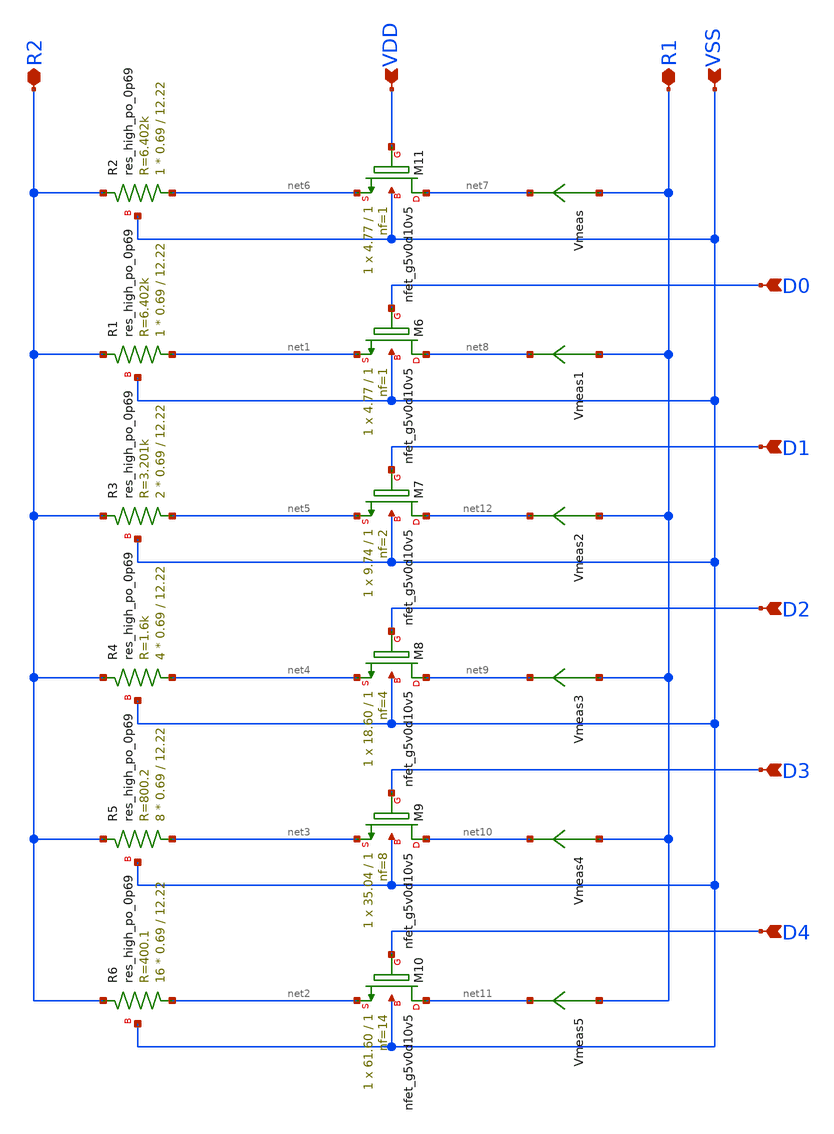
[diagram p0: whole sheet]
** sch_path: xschem/RB_array_20.sch
**.subckt RB_array_20 VSS R2 D0 D1 D2 D3 D4 R1 VDD
*.ipin VSS
*.iopin R2
*.ipin D0
*.ipin D1
*.ipin D2
*.ipin D3
*.ipin D4
*.iopin R1
*.ipin VDD
XR2 net6 R2 VSS sky130_fd_pr__res_high_po_0p69 L=12.22 mult=1 m=1
XR1 net1 R2 VSS sky130_fd_pr__res_high_po_0p69 L=12.22 mult=1 m=1
XR3 net5 R2 VSS sky130_fd_pr__res_high_po_0p69 L=12.22 mult=2 m=2
XR4 net4 R2 VSS sky130_fd_pr__res_high_po_0p69 L=12.22 mult=4 m=4
XR5 net3 R2 VSS sky130_fd_pr__res_high_po_0p69 L=12.22 mult=8 m=8
XR6 net2 R2 VSS sky130_fd_pr__res_high_po_0p69 L=12.22 mult=16 m=16
XM6 net8 D0 net1 VSS sky130_fd_pr__nfet_g5v0d10v5 L=1 W=4.77 nf=1 ad='int((nf+1)/2) * W/nf * 0.29' as='int((nf+2)/2) * W/nf * 0.29'
+ pd='2*int((nf+1)/2) * (W/nf + 0.29)' ps='2*int((nf+2)/2) * (W/nf + 0.29)' nrd='0.29 / W' nrs='0.29 / W'
+ sa=0 sb=0 sd=0 mult=1 m=1
XM7 net12 D1 net5 VSS sky130_fd_pr__nfet_g5v0d10v5 L=1 W=9.74 nf=2 ad='int((nf+1)/2) * W/nf * 0.29' as='int((nf+2)/2) * W/nf * 0.29'
+ pd='2*int((nf+1)/2) * (W/nf + 0.29)' ps='2*int((nf+2)/2) * (W/nf + 0.29)' nrd='0.29 / W' nrs='0.29 / W'
+ sa=0 sb=0 sd=0 mult=1 m=1
XM8 net9 D2 net4 VSS sky130_fd_pr__nfet_g5v0d10v5 L=1 W=18.60 nf=4 ad='int((nf+1)/2) * W/nf * 0.29' as='int((nf+2)/2) * W/nf * 0.29'
+ pd='2*int((nf+1)/2) * (W/nf + 0.29)' ps='2*int((nf+2)/2) * (W/nf + 0.29)' nrd='0.29 / W' nrs='0.29 / W'
+ sa=0 sb=0 sd=0 mult=1 m=1
XM9 net10 D3 net3 VSS sky130_fd_pr__nfet_g5v0d10v5 L=1 W=35.04 nf=8 ad='int((nf+1)/2) * W/nf * 0.29'
+ as='int((nf+2)/2) * W/nf * 0.29' pd='2*int((nf+1)/2) * (W/nf + 0.29)' ps='2*int((nf+2)/2) * (W/nf + 0.29)'
+ nrd='0.29 / W' nrs='0.29 / W' sa=0 sb=0 sd=0 mult=1 m=1
XM10 net11 D4 net2 VSS sky130_fd_pr__nfet_g5v0d10v5 L=1 W=61.60 nf=14 ad='int((nf+1)/2) * W/nf * 0.29'
+ as='int((nf+2)/2) * W/nf * 0.29' pd='2*int((nf+1)/2) * (W/nf + 0.29)' ps='2*int((nf+2)/2) * (W/nf + 0.29)'
+ nrd='0.29 / W' nrs='0.29 / W' sa=0 sb=0 sd=0 mult=1 m=1
XM11 net7 VDD net6 VSS sky130_fd_pr__nfet_g5v0d10v5 L=1 W=4.77 nf=1 ad='int((nf+1)/2) * W/nf * 0.29'
+ as='int((nf+2)/2) * W/nf * 0.29' pd='2*int((nf+1)/2) * (W/nf + 0.29)' ps='2*int((nf+2)/2) * (W/nf + 0.29)'
+ nrd='0.29 / W' nrs='0.29 / W' sa=0 sb=0 sd=0 mult=1 m=1
Vmeas R1 net7 0
.save i(vmeas)
Vmeas1 R1 net8 0
.save i(vmeas1)
Vmeas2 R1 net12 0
.save i(vmeas2)
Vmeas3 R1 net9 0
.save i(vmeas3)
Vmeas4 R1 net10 0
.save i(vmeas4)
Vmeas5 R1 net11 0
.save i(vmeas5)
**.ends
.end
